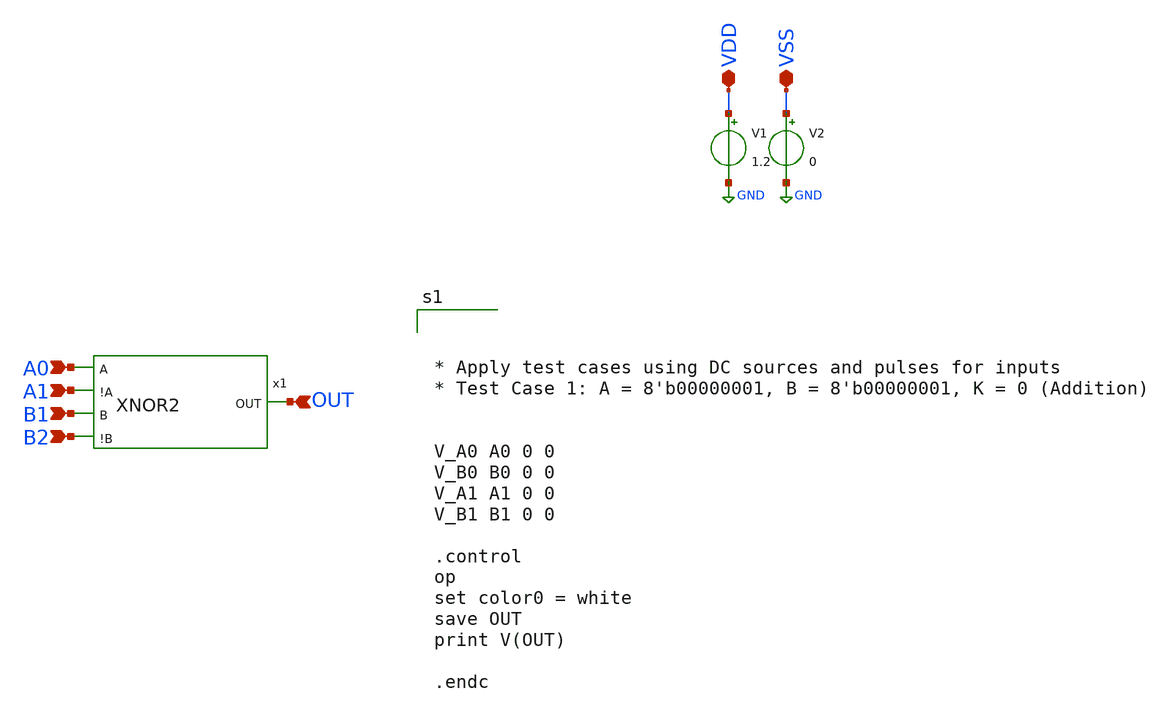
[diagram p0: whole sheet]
** sch_path: design/xschem/TEST_BENCHES/XNOR2_TB.sch
**.subckt XNOR2_TB VDD VSS A0 A1 B1 B2 OUT
*.iopin VDD
*.iopin VSS
*.ipin A0
*.ipin A1
*.ipin B1
*.ipin B2
*.ipin OUT
x1 A0 A1 B1 B2 OUT VSS VDD XNOR2
V1 VDD GND 1.2
V2 VSS GND 0
**** begin user architecture code

** opencircuitdesign pdks install
.lib $::SKYWATER_MODELS/sky130.lib.spice tt_mm





* Apply test cases using DC sources and pulses for inputs
* Test Case 1: A = 8'b00000001, B = 8'b00000001, K = 0 (Addition)


V_A0 A0 0 0
V_B0 B0 0 0
V_A1 A1 0 0
V_B1 B1 0 0

.control
op
set color0 = white
save OUT
print V(OUT)

.endc


**** end user architecture code
**.ends

* expanding   symbol:  XNOR/XNOR2.sym # of pins=5
** sym_path: design/xschem/XNOR/XNOR2.sym
** sch_path: design/xschem/XNOR/XNOR2.sch
.subckt XNOR2 A !A B !B OUT VSS VDD
*.ipin A
*.ipin !A
*.ipin B
*.ipin !B
*.opin OUT
x1 B !A !B A OUT !A A B !B VSS VDD cg4
.ends


* expanding   symbol:  ../CG4/cg4.sym # of pins=9
** sym_path: design/xschem/CG4/cg4.sym
** sch_path: design/xschem/CG4/cg4.sch
.subckt cg4 P3 P4 P2 P1 OUT N2 N1 N4 N3 VSS VDD
*.ipin P3
*.ipin P1
*.ipin N1
*.ipin N3
*.ipin P4
*.ipin P2
*.ipin N2
*.ipin N4
*.opin OUT
XM1 OUT N1 net1 VSS sky130_fd_pr__nfet_01v8 L=0.15 W=2 nf=1 ad='int((nf+1)/2) * W/nf * 0.29' as='int((nf+2)/2) * W/nf * 0.29'
+ pd='2*int((nf+1)/2) * (W/nf + 0.29)' ps='2*int((nf+2)/2) * (W/nf + 0.29)' nrd='0.29 / W' nrs='0.29 / W'
+ sa=0 sb=0 sd=0 mult=1 m=1
XM2 OUT N2 net2 VSS sky130_fd_pr__nfet_01v8 L=0.15 W=2 nf=1 ad='int((nf+1)/2) * W/nf * 0.29' as='int((nf+2)/2) * W/nf * 0.29'
+ pd='2*int((nf+1)/2) * (W/nf + 0.29)' ps='2*int((nf+2)/2) * (W/nf + 0.29)' nrd='0.29 / W' nrs='0.29 / W'
+ sa=0 sb=0 sd=0 mult=1 m=1
XM3 net1 N3 VSS VSS sky130_fd_pr__nfet_01v8 L=0.15 W=2 nf=1 ad='int((nf+1)/2) * W/nf * 0.29' as='int((nf+2)/2) * W/nf * 0.29'
+ pd='2*int((nf+1)/2) * (W/nf + 0.29)' ps='2*int((nf+2)/2) * (W/nf + 0.29)' nrd='0.29 / W' nrs='0.29 / W'
+ sa=0 sb=0 sd=0 mult=1 m=1
XM4 net2 N4 VSS VSS sky130_fd_pr__nfet_01v8 L=0.15 W=2 nf=1 ad='int((nf+1)/2) * W/nf * 0.29' as='int((nf+2)/2) * W/nf * 0.29'
+ pd='2*int((nf+1)/2) * (W/nf + 0.29)' ps='2*int((nf+2)/2) * (W/nf + 0.29)' nrd='0.29 / W' nrs='0.29 / W'
+ sa=0 sb=0 sd=0 mult=1 m=1
XM5 OUT P1 net3 VDD sky130_fd_pr__pfet_01v8 L=0.15 W=8.25 nf=1 ad='int((nf+1)/2) * W/nf * 0.29' as='int((nf+2)/2) * W/nf * 0.29'
+ pd='2*int((nf+1)/2) * (W/nf + 0.29)' ps='2*int((nf+2)/2) * (W/nf + 0.29)' nrd='0.29 / W' nrs='0.29 / W'
+ sa=0 sb=0 sd=0 mult=1 m=1
XM6 OUT P2 net3 VDD sky130_fd_pr__pfet_01v8 L=0.15 W=8.25 nf=1 ad='int((nf+1)/2) * W/nf * 0.29' as='int((nf+2)/2) * W/nf * 0.29'
+ pd='2*int((nf+1)/2) * (W/nf + 0.29)' ps='2*int((nf+2)/2) * (W/nf + 0.29)' nrd='0.29 / W' nrs='0.29 / W'
+ sa=0 sb=0 sd=0 mult=1 m=1
XM7 net3 P3 VDD VDD sky130_fd_pr__pfet_01v8 L=0.15 W=8.25 nf=1 ad='int((nf+1)/2) * W/nf * 0.29' as='int((nf+2)/2) * W/nf * 0.29'
+ pd='2*int((nf+1)/2) * (W/nf + 0.29)' ps='2*int((nf+2)/2) * (W/nf + 0.29)' nrd='0.29 / W' nrs='0.29 / W'
+ sa=0 sb=0 sd=0 mult=1 m=1
XM8 net3 P4 VDD VDD sky130_fd_pr__pfet_01v8 L=0.15 W=8.25 nf=1 ad='int((nf+1)/2) * W/nf * 0.29' as='int((nf+2)/2) * W/nf * 0.29'
+ pd='2*int((nf+1)/2) * (W/nf + 0.29)' ps='2*int((nf+2)/2) * (W/nf + 0.29)' nrd='0.29 / W' nrs='0.29 / W'
+ sa=0 sb=0 sd=0 mult=1 m=1
.ends

.GLOBAL GND
.end
